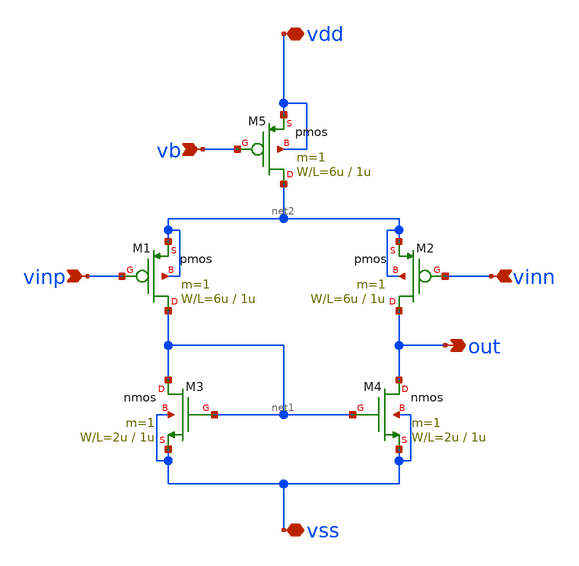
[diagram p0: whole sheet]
** sch_path: OR1/PTC06/opamp/diff-stage.sch
**.subckt diff-stage vinp vinn vb out vdd vss
*.ipin vinp
*.ipin vinn
*.ipin vb
*.opin out
*.iopin vdd
*.iopin vss
M5 net2 vb vdd vdd pmos L=1u W=6u m=1
M1 net1 vinp net2 net2 pmos L=1u W=6u m=1
M2 out vinn net2 net2 pmos L=1u W=6u m=1
M3 net1 net1 vss vss nmos L=1u W=2u m=1
M4 out net1 vss vss nmos L=1u W=2u m=1
**.ends
.end
